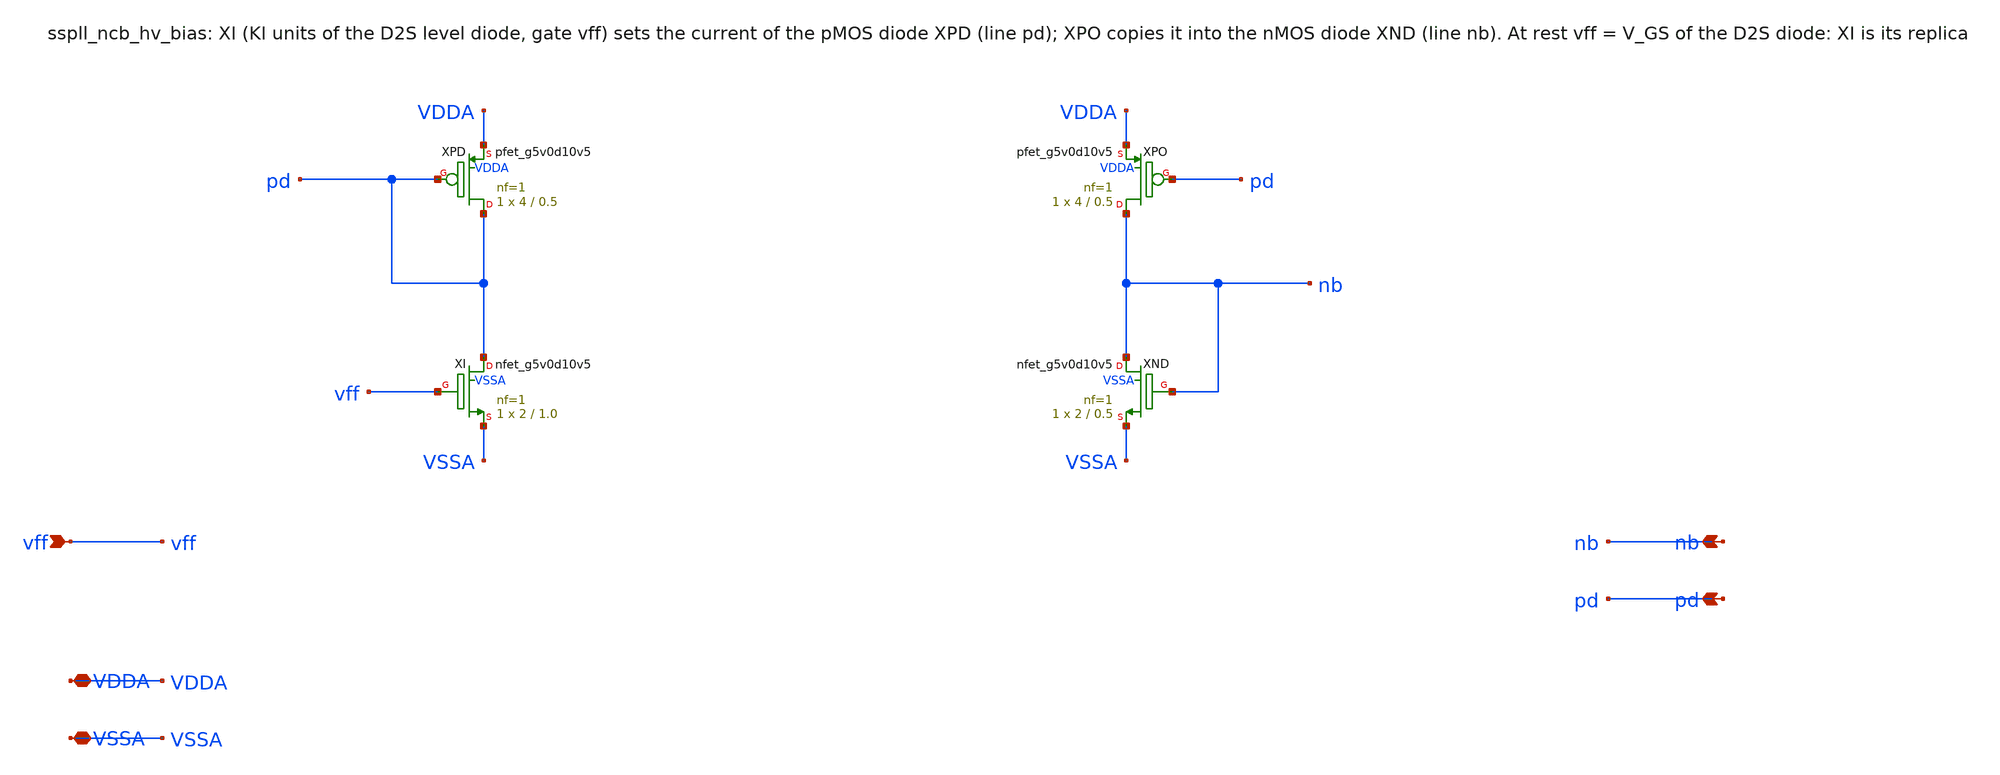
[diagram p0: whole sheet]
** sch_path: xschem/ncb_hv/sspll_ncb_hv_bias.sch
**.subckt sspll_ncb_hv_bias vff nb pd VDDA VSSA
*.ipin vff
*.opin nb
*.opin pd
*.iopin VDDA
*.iopin VSSA
XXPD pd pd VDDA VDDA sky130_fd_pr__pfet_g5v0d10v5 L=0.5 W=4 nf=1 ad='int((nf+1)/2) * W/nf * 0.29' as='int((nf+2)/2) * W/nf * 0.29'
+ pd='2*int((nf+1)/2) * (W/nf + 0.29)' ps='2*int((nf+2)/2) * (W/nf + 0.29)' nrd='0.29 / W' nrs='0.29 / W'
+ sa=0 sb=0 sd=0 mult=1 m=1
XXI pd vff VSSA VSSA sky130_fd_pr__nfet_g5v0d10v5 L=1.0 W=2 nf=1 ad='int((nf+1)/2) * W/nf * 0.29' as='int((nf+2)/2) * W/nf * 0.29'
+ pd='2*int((nf+1)/2) * (W/nf + 0.29)' ps='2*int((nf+2)/2) * (W/nf + 0.29)' nrd='0.29 / W' nrs='0.29 / W'
+ sa=0 sb=0 sd=0 mult=1 m=1
XXPO nb pd VDDA VDDA sky130_fd_pr__pfet_g5v0d10v5 L=0.5 W=4 nf=1 ad='int((nf+1)/2) * W/nf * 0.29' as='int((nf+2)/2) * W/nf * 0.29'
+ pd='2*int((nf+1)/2) * (W/nf + 0.29)' ps='2*int((nf+2)/2) * (W/nf + 0.29)' nrd='0.29 / W' nrs='0.29 / W'
+ sa=0 sb=0 sd=0 mult=1 m=1
XXND nb nb VSSA VSSA sky130_fd_pr__nfet_g5v0d10v5 L=0.5 W=2 nf=1 ad='int((nf+1)/2) * W/nf * 0.29' as='int((nf+2)/2) * W/nf * 0.29'
+ pd='2*int((nf+1)/2) * (W/nf + 0.29)' ps='2*int((nf+2)/2) * (W/nf + 0.29)' nrd='0.29 / W' nrs='0.29 / W'
+ sa=0 sb=0 sd=0 mult=1 m=1
**.ends
.end
